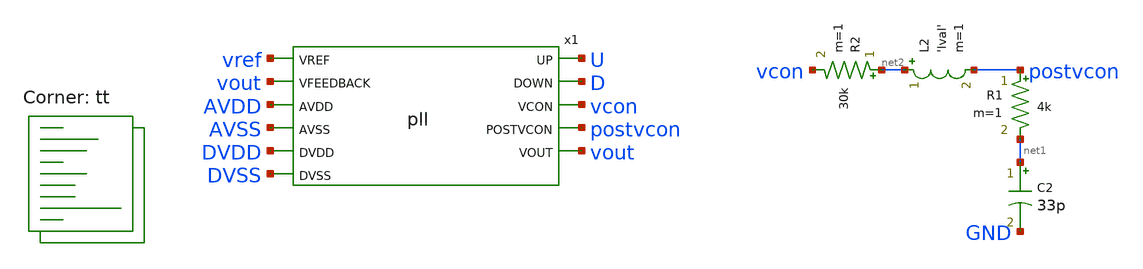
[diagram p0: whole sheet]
** sch_path: xschem/pll-tb.sch
**.subckt pll-tb
R1 postvcon net1 4k m=1
R2 net2 vcon 30k m=1
C2 net1 GND 33p m=1
x1 vref vout AVDD AVSS DVDD DVSS U D vcon postvcon vout pll
L2 net2 postvcon 'lval' m=1
**** begin user architecture code
 .lib $::SKYWATER_MODELS/sky130.lib.spice tt
.include $::SKYWATER_STDCELLS/sky130_fd_sc_hd.spice
.param mc_mm_switch = 0
.param mc_pr_switch = 0




  .param max_freq=100e6 period={1/max_freq} time_high={period/2}
  .param delay_vin1={time_high} delay_vin2={time_high*1.5}
  .param lval=100u

  .option wnflag=1
  .option safecurrents

  Vavdd AVDD AVSS dc 1.8
  Vavss AVSS GND dc 0
  Vdvdd DVDD DVSS dc 1.8
  Vdvss DVSS GND dc 0

  Vref vref GND pulse(0 1.8 {delay_vin1} 1p 1p {time_high} {period})

  .control
     reset
     save vref vfeed u d vcon postvcon vout
     tran 0.01n 5u uic
     write pll-tb.raw
     set appendwrite

     alterparam max_freq=8e6
     reset
     save vref vfeed u d vcon postvcon vout
     tran 0.01n 5u uic
     write pll-tb.raw
    quit 0
  .endc



**** end user architecture code
**.ends

* expanding   symbol:  pll.sym # of pins=11
** sym_path: xschem/pll.sym
** sch_path: xschem/pll.sch
.subckt pll VREF VFEEDBACK AVDD AVSS DVDD DVSS UP DOWN VCON POSTVCON VOUT
*.ipin VREF
*.ipin VFEEDBACK
*.ipin AVDD
*.ipin AVSS
*.ipin DVDD
*.ipin DVSS
*.opin UP
*.opin DOWN
*.opin VCON
*.opin POSTVCON
*.opin VOUT
x1 VREF VFEEDBACK UP DOWN DVDD DVSS pfd
x3 POSTVCON VOUT AVDD AVSS vco
x2 net1 UP net2 DOWN AVDD AVSS net3 charge_pump
.ends


* expanding   symbol:  pfd.sym # of pins=6
** sym_path: xschem/pfd.sym
** sch_path: xschem/pfd.sch
.subckt pfd vin1 vin2 U D VDD GND
*.ipin vin1
*.ipin vin2
*.opin U
*.opin D
*.ipin VDD
*.ipin GND
.param wpmos=1.26 lpmos=0.15 wnmos=0.42 lnmos=0.15 wpand=1.5

XM1 net4 rst GND GND sky130_fd_pr__nfet_01v8 L=lnmos W=wnmos nf=1 ad='int((nf+1)/2) * W/nf * 0.29' as='int((nf+2)/2) * W/nf * 0.29'
+ pd='2*int((nf+1)/2) * (W/nf + 0.29)' ps='2*int((nf+2)/2) * (W/nf + 0.29)' nrd='0.29 / W' nrs='0.29 / W'
+ sa=0 sb=0 sd=0 mult=1 m=1
XM2 net3 vin1 VDD VDD sky130_fd_pr__pfet_01v8 L=lpmos W=wpmos nf=1 ad='int((nf+1)/2) * W/nf * 0.29' as='int((nf+2)/2) * W/nf * 0.29'
+ pd='2*int((nf+1)/2) * (W/nf + 0.29)' ps='2*int((nf+2)/2) * (W/nf + 0.29)' nrd='0.29 / W' nrs='0.29 / W'
+ sa=0 sb=0 sd=0 mult=1 m=1
XM3 net4 rst net3 VDD sky130_fd_pr__pfet_01v8 L=lpmos W=wpmos nf=1 ad='int((nf+1)/2) * W/nf * 0.29' as='int((nf+2)/2) * W/nf * 0.29'
+ pd='2*int((nf+1)/2) * (W/nf + 0.29)' ps='2*int((nf+2)/2) * (W/nf + 0.29)' nrd='0.29 / W' nrs='0.29 / W'
+ sa=0 sb=0 sd=0 mult=1 m=1
XM4 net1 net4 VDD VDD sky130_fd_pr__pfet_01v8 L=lpmos W=wpmos nf=1 ad='int((nf+1)/2) * W/nf * 0.29' as='int((nf+2)/2) * W/nf * 0.29'
+ pd='2*int((nf+1)/2) * (W/nf + 0.29)' ps='2*int((nf+2)/2) * (W/nf + 0.29)' nrd='0.29 / W' nrs='0.29 / W'
+ sa=0 sb=0 sd=0 mult=1 m=1
XM5 preU net1 VDD VDD sky130_fd_pr__pfet_01v8 L=lpmos W=wpmos nf=1 ad='int((nf+1)/2) * W/nf * 0.29' as='int((nf+2)/2) * W/nf * 0.29'
+ pd='2*int((nf+1)/2) * (W/nf + 0.29)' ps='2*int((nf+2)/2) * (W/nf + 0.29)' nrd='0.29 / W' nrs='0.29 / W'
+ sa=0 sb=0 sd=0 mult=1 m=1
XM6 net1 net4 net2 GND sky130_fd_pr__nfet_01v8 L=lnmos W=wnmos nf=1 ad='int((nf+1)/2) * W/nf * 0.29'
+ as='int((nf+2)/2) * W/nf * 0.29' pd='2*int((nf+1)/2) * (W/nf + 0.29)' ps='2*int((nf+2)/2) * (W/nf + 0.29)'
+ nrd='0.29 / W' nrs='0.29 / W' sa=0 sb=0 sd=0 mult=1 m=1
XM7 preU net1 GND GND sky130_fd_pr__nfet_01v8 L=lnmos W=wnmos nf=1 ad='int((nf+1)/2) * W/nf * 0.29' as='int((nf+2)/2) * W/nf * 0.29'
+ pd='2*int((nf+1)/2) * (W/nf + 0.29)' ps='2*int((nf+2)/2) * (W/nf + 0.29)' nrd='0.29 / W' nrs='0.29 / W'
+ sa=0 sb=0 sd=0 mult=1 m=1
XM8 net2 vin1 GND GND sky130_fd_pr__nfet_01v8 L=lnmos W=wnmos nf=1 ad='int((nf+1)/2) * W/nf * 0.29' as='int((nf+2)/2) * W/nf * 0.29'
+ pd='2*int((nf+1)/2) * (W/nf + 0.29)' ps='2*int((nf+2)/2) * (W/nf + 0.29)' nrd='0.29 / W' nrs='0.29 / W'
+ sa=0 sb=0 sd=0 mult=1 m=1
XM10 net6 vin2 VDD VDD sky130_fd_pr__pfet_01v8 L=lpmos W=wpmos nf=1 ad='int((nf+1)/2) * W/nf * 0.29'
+ as='int((nf+2)/2) * W/nf * 0.29' pd='2*int((nf+1)/2) * (W/nf + 0.29)' ps='2*int((nf+2)/2) * (W/nf + 0.29)'
+ nrd='0.29 / W' nrs='0.29 / W' sa=0 sb=0 sd=0 mult=1 m=1
XM11 net5 net7 VDD VDD sky130_fd_pr__pfet_01v8 L=lpmos W=wpmos nf=1 ad='int((nf+1)/2) * W/nf * 0.29'
+ as='int((nf+2)/2) * W/nf * 0.29' pd='2*int((nf+1)/2) * (W/nf + 0.29)' ps='2*int((nf+2)/2) * (W/nf + 0.29)'
+ nrd='0.29 / W' nrs='0.29 / W' sa=0 sb=0 sd=0 mult=1 m=1
XM12 net7 rst net6 VDD sky130_fd_pr__pfet_01v8 L=lpmos W=wpmos nf=1 ad='int((nf+1)/2) * W/nf * 0.29'
+ as='int((nf+2)/2) * W/nf * 0.29' pd='2*int((nf+1)/2) * (W/nf + 0.29)' ps='2*int((nf+2)/2) * (W/nf + 0.29)'
+ nrd='0.29 / W' nrs='0.29 / W' sa=0 sb=0 sd=0 mult=1 m=1
XM13 preD net5 VDD VDD sky130_fd_pr__pfet_01v8 L=lpmos W=wpmos nf=1 ad='int((nf+1)/2) * W/nf * 0.29'
+ as='int((nf+2)/2) * W/nf * 0.29' pd='2*int((nf+1)/2) * (W/nf + 0.29)' ps='2*int((nf+2)/2) * (W/nf + 0.29)'
+ nrd='0.29 / W' nrs='0.29 / W' sa=0 sb=0 sd=0 mult=1 m=1
XM14 net7 rst GND GND sky130_fd_pr__nfet_01v8 L=lnmos W=wnmos nf=1 ad='int((nf+1)/2) * W/nf * 0.29' as='int((nf+2)/2) * W/nf * 0.29'
+ pd='2*int((nf+1)/2) * (W/nf + 0.29)' ps='2*int((nf+2)/2) * (W/nf + 0.29)' nrd='0.29 / W' nrs='0.29 / W'
+ sa=0 sb=0 sd=0 mult=1 m=1
XM15 net5 net7 net8 GND sky130_fd_pr__nfet_01v8 L=lnmos W=wnmos nf=1 ad='int((nf+1)/2) * W/nf * 0.29'
+ as='int((nf+2)/2) * W/nf * 0.29' pd='2*int((nf+1)/2) * (W/nf + 0.29)' ps='2*int((nf+2)/2) * (W/nf + 0.29)'
+ nrd='0.29 / W' nrs='0.29 / W' sa=0 sb=0 sd=0 mult=1 m=1
XM16 preD net5 GND GND sky130_fd_pr__nfet_01v8 L=lnmos W=wnmos nf=1 ad='int((nf+1)/2) * W/nf * 0.29'
+ as='int((nf+2)/2) * W/nf * 0.29' pd='2*int((nf+1)/2) * (W/nf + 0.29)' ps='2*int((nf+2)/2) * (W/nf + 0.29)'
+ nrd='0.29 / W' nrs='0.29 / W' sa=0 sb=0 sd=0 mult=1 m=1
XM18 net8 vin2 GND GND sky130_fd_pr__nfet_01v8 L=lnmos W=wnmos nf=1 ad='int((nf+1)/2) * W/nf * 0.29'
+ as='int((nf+2)/2) * W/nf * 0.29' pd='2*int((nf+1)/2) * (W/nf + 0.29)' ps='2*int((nf+2)/2) * (W/nf + 0.29)'
+ nrd='0.29 / W' nrs='0.29 / W' sa=0 sb=0 sd=0 mult=1 m=1
x1 preU GND GND VDD VDD U sky130_fd_sc_hd__buf_8
x2 preD GND GND VDD VDD D sky130_fd_sc_hd__buf_8
x3 prerst GND GND VDD VDD rst sky130_fd_sc_hd__buf_1
x4 U D GND GND VDD VDD prerst sky130_fd_sc_hd__and2_1
.ends


* expanding   symbol:  vco.sym # of pins=4
** sym_path: xschem/vco.sym
** sch_path: xschem/vco.sch
.subckt vco VCON VOUT AVDD AVSS
*.ipin VCON
*.opin VOUT
*.ipin AVDD
*.ipin AVSS
.param wpo=4.8 lpo=0.54 wno=2.4 lno=0.54 wpcb=4.8 lpcb=0.36 wncb=0.96 lncb=0.36 wpvb=6 lpvb=0.9
+ wnvc=96 lnvc=0.9 wpbuff=4.8 lpbuff=0.18 wnbuff=1.2 lnbuff=0.18 lres=3.5

XM1 vnbias vnbias AVSS AVSS sky130_fd_pr__nfet_01v8 L=lncb W=wncb nf=1 ad='int((nf+1)/2) * W/nf * 0.29'
+ as='int((nf+2)/2) * W/nf * 0.29' pd='2*int((nf+1)/2) * (W/nf + 0.29)' ps='2*int((nf+2)/2) * (W/nf + 0.29)'
+ nrd='0.29 / W' nrs='0.29 / W' sa=0 sb=0 sd=0 mult=1 m=1
XM2 vpbias vpbias AVDD AVDD sky130_fd_pr__pfet_01v8 L=lpvb W=wpvb nf=1 ad='int((nf+1)/2) * W/nf * 0.29'
+ as='int((nf+2)/2) * W/nf * 0.29' pd='2*int((nf+1)/2) * (W/nf + 0.29)' ps='2*int((nf+2)/2) * (W/nf + 0.29)'
+ nrd='0.29 / W' nrs='0.29 / W' sa=0 sb=0 sd=0 mult=1 m=1
XM4 vnbias vpbias AVDD AVDD sky130_fd_pr__pfet_01v8 L=lpcb W=wpcb nf=1 ad='int((nf+1)/2) * W/nf * 0.29'
+ as='int((nf+2)/2) * W/nf * 0.29' pd='2*int((nf+1)/2) * (W/nf + 0.29)' ps='2*int((nf+2)/2) * (W/nf + 0.29)'
+ nrd='0.29 / W' nrs='0.29 / W' sa=0 sb=0 sd=0 mult=1 m=1
XM5 net8 net9 net1 AVSS sky130_fd_pr__nfet_01v8 L=lno W=wno nf=1 ad='int((nf+1)/2) * W/nf * 0.29' as='int((nf+2)/2) * W/nf * 0.29'
+ pd='2*int((nf+1)/2) * (W/nf + 0.29)' ps='2*int((nf+2)/2) * (W/nf + 0.29)' nrd='0.29 / W' nrs='0.29 / W'
+ sa=0 sb=0 sd=0 mult=1 m=1
XM6 net8 net9 net12 AVDD sky130_fd_pr__pfet_01v8 L=lpo W=wpo nf=1 ad='int((nf+1)/2) * W/nf * 0.29' as='int((nf+2)/2) * W/nf * 0.29'
+ pd='2*int((nf+1)/2) * (W/nf + 0.29)' ps='2*int((nf+2)/2) * (W/nf + 0.29)' nrd='0.29 / W' nrs='0.29 / W'
+ sa=0 sb=0 sd=0 mult=1 m=1
XM7 net7 net8 net2 AVSS sky130_fd_pr__nfet_01v8 L=lno W=wno nf=1 ad='int((nf+1)/2) * W/nf * 0.29' as='int((nf+2)/2) * W/nf * 0.29'
+ pd='2*int((nf+1)/2) * (W/nf + 0.29)' ps='2*int((nf+2)/2) * (W/nf + 0.29)' nrd='0.29 / W' nrs='0.29 / W'
+ sa=0 sb=0 sd=0 mult=1 m=1
XM8 net7 net8 net13 AVDD sky130_fd_pr__pfet_01v8 L=lpo W=wpo nf=1 ad='int((nf+1)/2) * W/nf * 0.29' as='int((nf+2)/2) * W/nf * 0.29'
+ pd='2*int((nf+1)/2) * (W/nf + 0.29)' ps='2*int((nf+2)/2) * (W/nf + 0.29)' nrd='0.29 / W' nrs='0.29 / W'
+ sa=0 sb=0 sd=0 mult=1 m=1
XM9 net6 net7 net3 AVSS sky130_fd_pr__nfet_01v8 L=lno W=wno nf=1 ad='int((nf+1)/2) * W/nf * 0.29' as='int((nf+2)/2) * W/nf * 0.29'
+ pd='2*int((nf+1)/2) * (W/nf + 0.29)' ps='2*int((nf+2)/2) * (W/nf + 0.29)' nrd='0.29 / W' nrs='0.29 / W'
+ sa=0 sb=0 sd=0 mult=1 m=1
XM10 net6 net7 net14 AVDD sky130_fd_pr__pfet_01v8 L=lpo W=wpo nf=1 ad='int((nf+1)/2) * W/nf * 0.29' as='int((nf+2)/2) * W/nf * 0.29'
+ pd='2*int((nf+1)/2) * (W/nf + 0.29)' ps='2*int((nf+2)/2) * (W/nf + 0.29)' nrd='0.29 / W' nrs='0.29 / W'
+ sa=0 sb=0 sd=0 mult=1 m=1
XM11 net10 net6 net5 AVSS sky130_fd_pr__nfet_01v8 L=lno W=wno nf=1 ad='int((nf+1)/2) * W/nf * 0.29' as='int((nf+2)/2) * W/nf * 0.29'
+ pd='2*int((nf+1)/2) * (W/nf + 0.29)' ps='2*int((nf+2)/2) * (W/nf + 0.29)' nrd='0.29 / W' nrs='0.29 / W'
+ sa=0 sb=0 sd=0 mult=1 m=1
XM12 net10 net6 net15 AVDD sky130_fd_pr__pfet_01v8 L=lpo W=wpo nf=1 ad='int((nf+1)/2) * W/nf * 0.29'
+ as='int((nf+2)/2) * W/nf * 0.29' pd='2*int((nf+1)/2) * (W/nf + 0.29)' ps='2*int((nf+2)/2) * (W/nf + 0.29)'
+ nrd='0.29 / W' nrs='0.29 / W' sa=0 sb=0 sd=0 mult=1 m=1
XM13 net9 net10 net4 AVSS sky130_fd_pr__nfet_01v8 L=lno W=wno nf=1 ad='int((nf+1)/2) * W/nf * 0.29' as='int((nf+2)/2) * W/nf * 0.29'
+ pd='2*int((nf+1)/2) * (W/nf + 0.29)' ps='2*int((nf+2)/2) * (W/nf + 0.29)' nrd='0.29 / W' nrs='0.29 / W'
+ sa=0 sb=0 sd=0 mult=1 m=1
XM14 net9 net10 net16 AVDD sky130_fd_pr__pfet_01v8 L=lpo W=wpo nf=1 ad='int((nf+1)/2) * W/nf * 0.29'
+ as='int((nf+2)/2) * W/nf * 0.29' pd='2*int((nf+1)/2) * (W/nf + 0.29)' ps='2*int((nf+2)/2) * (W/nf + 0.29)'
+ nrd='0.29 / W' nrs='0.29 / W' sa=0 sb=0 sd=0 mult=1 m=1
XM16 net12 vpbias AVDD AVDD sky130_fd_pr__pfet_01v8 L=lpcb W=wpcb nf=1 ad='int((nf+1)/2) * W/nf * 0.29'
+ as='int((nf+2)/2) * W/nf * 0.29' pd='2*int((nf+1)/2) * (W/nf + 0.29)' ps='2*int((nf+2)/2) * (W/nf + 0.29)'
+ nrd='0.29 / W' nrs='0.29 / W' sa=0 sb=0 sd=0 mult=1 m=1
XM18 net13 vpbias AVDD AVDD sky130_fd_pr__pfet_01v8 L=lpcb W=wpcb nf=1 ad='int((nf+1)/2) * W/nf * 0.29'
+ as='int((nf+2)/2) * W/nf * 0.29' pd='2*int((nf+1)/2) * (W/nf + 0.29)' ps='2*int((nf+2)/2) * (W/nf + 0.29)'
+ nrd='0.29 / W' nrs='0.29 / W' sa=0 sb=0 sd=0 mult=1 m=1
XM20 net14 vpbias AVDD AVDD sky130_fd_pr__pfet_01v8 L=lpcb W=wpcb nf=1 ad='int((nf+1)/2) * W/nf * 0.29'
+ as='int((nf+2)/2) * W/nf * 0.29' pd='2*int((nf+1)/2) * (W/nf + 0.29)' ps='2*int((nf+2)/2) * (W/nf + 0.29)'
+ nrd='0.29 / W' nrs='0.29 / W' sa=0 sb=0 sd=0 mult=1 m=1
XM22 net15 vpbias AVDD AVDD sky130_fd_pr__pfet_01v8 L=lpcb W=wpcb nf=1 ad='int((nf+1)/2) * W/nf * 0.29'
+ as='int((nf+2)/2) * W/nf * 0.29' pd='2*int((nf+1)/2) * (W/nf + 0.29)' ps='2*int((nf+2)/2) * (W/nf + 0.29)'
+ nrd='0.29 / W' nrs='0.29 / W' sa=0 sb=0 sd=0 mult=1 m=1
XM24 net16 vpbias AVDD AVDD sky130_fd_pr__pfet_01v8 L=lpcb W=wpcb nf=1 ad='int((nf+1)/2) * W/nf * 0.29'
+ as='int((nf+2)/2) * W/nf * 0.29' pd='2*int((nf+1)/2) * (W/nf + 0.29)' ps='2*int((nf+2)/2) * (W/nf + 0.29)'
+ nrd='0.29 / W' nrs='0.29 / W' sa=0 sb=0 sd=0 mult=1 m=1
XM25 net11 net9 AVSS AVSS sky130_fd_pr__nfet_01v8 L=lnbuff W=wnbuff nf=1 ad='int((nf+1)/2) * W/nf * 0.29'
+ as='int((nf+2)/2) * W/nf * 0.29' pd='2*int((nf+1)/2) * (W/nf + 0.29)' ps='2*int((nf+2)/2) * (W/nf + 0.29)'
+ nrd='0.29 / W' nrs='0.29 / W' sa=0 sb=0 sd=0 mult=1 m=1
XM26 net11 net9 AVDD AVDD sky130_fd_pr__pfet_01v8 L=lpbuff W=wpbuff nf=1 ad='int((nf+1)/2) * W/nf * 0.29'
+ as='int((nf+2)/2) * W/nf * 0.29' pd='2*int((nf+1)/2) * (W/nf + 0.29)' ps='2*int((nf+2)/2) * (W/nf + 0.29)'
+ nrd='0.29 / W' nrs='0.29 / W' sa=0 sb=0 sd=0 mult=1 m=1
XM27 VOUT net11 AVSS AVSS sky130_fd_pr__nfet_01v8 L=lnbuff W=wnbuff nf=1 ad='int((nf+1)/2) * W/nf * 0.29'
+ as='int((nf+2)/2) * W/nf * 0.29' pd='2*int((nf+1)/2) * (W/nf + 0.29)' ps='2*int((nf+2)/2) * (W/nf + 0.29)'
+ nrd='0.29 / W' nrs='0.29 / W' sa=0 sb=0 sd=0 mult=1 m=1
XM28 VOUT net11 AVDD AVDD sky130_fd_pr__pfet_01v8 L=lpbuff W=wpbuff nf=1 ad='int((nf+1)/2) * W/nf * 0.29'
+ as='int((nf+2)/2) * W/nf * 0.29' pd='2*int((nf+1)/2) * (W/nf + 0.29)' ps='2*int((nf+2)/2) * (W/nf + 0.29)'
+ nrd='0.29 / W' nrs='0.29 / W' sa=0 sb=0 sd=0 mult=1 m=1
XM15 net1 vnbias AVSS AVSS sky130_fd_pr__nfet_01v8 L=lncb W=wncb nf=1 ad='int((nf+1)/2) * W/nf * 0.29'
+ as='int((nf+2)/2) * W/nf * 0.29' pd='2*int((nf+1)/2) * (W/nf + 0.29)' ps='2*int((nf+2)/2) * (W/nf + 0.29)'
+ nrd='0.29 / W' nrs='0.29 / W' sa=0 sb=0 sd=0 mult=1 m=1
XM17 net2 vnbias AVSS AVSS sky130_fd_pr__nfet_01v8 L=lncb W=wncb nf=1 ad='int((nf+1)/2) * W/nf * 0.29'
+ as='int((nf+2)/2) * W/nf * 0.29' pd='2*int((nf+1)/2) * (W/nf + 0.29)' ps='2*int((nf+2)/2) * (W/nf + 0.29)'
+ nrd='0.29 / W' nrs='0.29 / W' sa=0 sb=0 sd=0 mult=1 m=1
XM19 net3 vnbias AVSS AVSS sky130_fd_pr__nfet_01v8 L=lncb W=wncb nf=1 ad='int((nf+1)/2) * W/nf * 0.29'
+ as='int((nf+2)/2) * W/nf * 0.29' pd='2*int((nf+1)/2) * (W/nf + 0.29)' ps='2*int((nf+2)/2) * (W/nf + 0.29)'
+ nrd='0.29 / W' nrs='0.29 / W' sa=0 sb=0 sd=0 mult=1 m=1
XM21 net5 vnbias AVSS AVSS sky130_fd_pr__nfet_01v8 L=lncb W=wncb nf=1 ad='int((nf+1)/2) * W/nf * 0.29'
+ as='int((nf+2)/2) * W/nf * 0.29' pd='2*int((nf+1)/2) * (W/nf + 0.29)' ps='2*int((nf+2)/2) * (W/nf + 0.29)'
+ nrd='0.29 / W' nrs='0.29 / W' sa=0 sb=0 sd=0 mult=1 m=1
XM23 net4 vnbias AVSS AVSS sky130_fd_pr__nfet_01v8 L=lncb W=wncb nf=1 ad='int((nf+1)/2) * W/nf * 0.29'
+ as='int((nf+2)/2) * W/nf * 0.29' pd='2*int((nf+1)/2) * (W/nf + 0.29)' ps='2*int((nf+2)/2) * (W/nf + 0.29)'
+ nrd='0.29 / W' nrs='0.29 / W' sa=0 sb=0 sd=0 mult=1 m=1
XR3 AVSS net17 AVSS sky130_fd_pr__res_xhigh_po W=0.35 L=lres mult=1 m=1
XM29 vpbias VCON net17 AVSS sky130_fd_pr__nfet_01v8 L=lnvc W=wnvc nf=1 ad='int((nf+1)/2) * W/nf * 0.29'
+ as='int((nf+2)/2) * W/nf * 0.29' pd='2*int((nf+1)/2) * (W/nf + 0.29)' ps='2*int((nf+2)/2) * (W/nf + 0.29)'
+ nrd='0.29 / W' nrs='0.29 / W' sa=0 sb=0 sd=0 mult=1 m=1
.ends


* expanding   symbol:  charge_pump.sym # of pins=7
** sym_path: xschem/charge_pump.sym
** sch_path: xschem/charge_pump.sch
.subckt charge_pump U D vcon AVDD AVSS DVDD DVSS
*.ipin U
*.ipin D
*.opin vcon
*.ipin AVDD
*.ipin AVSS
*.ipin DVDD
*.ipin DVSS
XM1 vcon Ub AVDD AVDD sky130_fd_pr__pfet_01v8 L=0.5 W=2.5 nf=1 ad='int((nf+1)/2) * W/nf * 0.29' as='int((nf+2)/2) * W/nf * 0.29'
+ pd='2*int((nf+1)/2) * (W/nf + 0.29)' ps='2*int((nf+2)/2) * (W/nf + 0.29)' nrd='0.29 / W' nrs='0.29 / W'
+ sa=0 sb=0 sd=0 mult=4 m=4
XM2 vcon net1 AVSS AVSS sky130_fd_pr__nfet_01v8 L=0.5 W=2.5 nf=1 ad='int((nf+1)/2) * W/nf * 0.29' as='int((nf+2)/2) * W/nf * 0.29'
+ pd='2*int((nf+1)/2) * (W/nf + 0.29)' ps='2*int((nf+2)/2) * (W/nf + 0.29)' nrd='0.29 / W' nrs='0.29 / W'
+ sa=0 sb=0 sd=0 mult=4 m=4
x1 D DVSS DVSS DVDD DVDD net1 sky130_fd_sc_hd__buf_1
x2 U DVSS DVSS DVDD DVDD Ub sky130_fd_sc_hd__inv_1
XM3 AVDD AVDD AVDD AVDD sky130_fd_pr__pfet_01v8 L=0.15 W=2.5 nf=1 ad='int((nf+1)/2) * W/nf * 0.29' as='int((nf+2)/2) * W/nf * 0.29'
+ pd='2*int((nf+1)/2) * (W/nf + 0.29)' ps='2*int((nf+2)/2) * (W/nf + 0.29)' nrd='0.29 / W' nrs='0.29 / W'
+ sa=0 sb=0 sd=0 mult=4 m=4
XM4 AVSS AVSS AVSS AVSS sky130_fd_pr__nfet_01v8 L=0.15 W=2.5 nf=1 ad='int((nf+1)/2) * W/nf * 0.29' as='int((nf+2)/2) * W/nf * 0.29'
+ pd='2*int((nf+1)/2) * (W/nf + 0.29)' ps='2*int((nf+2)/2) * (W/nf + 0.29)' nrd='0.29 / W' nrs='0.29 / W'
+ sa=0 sb=0 sd=0 mult=4 m=4
.ends

.end
